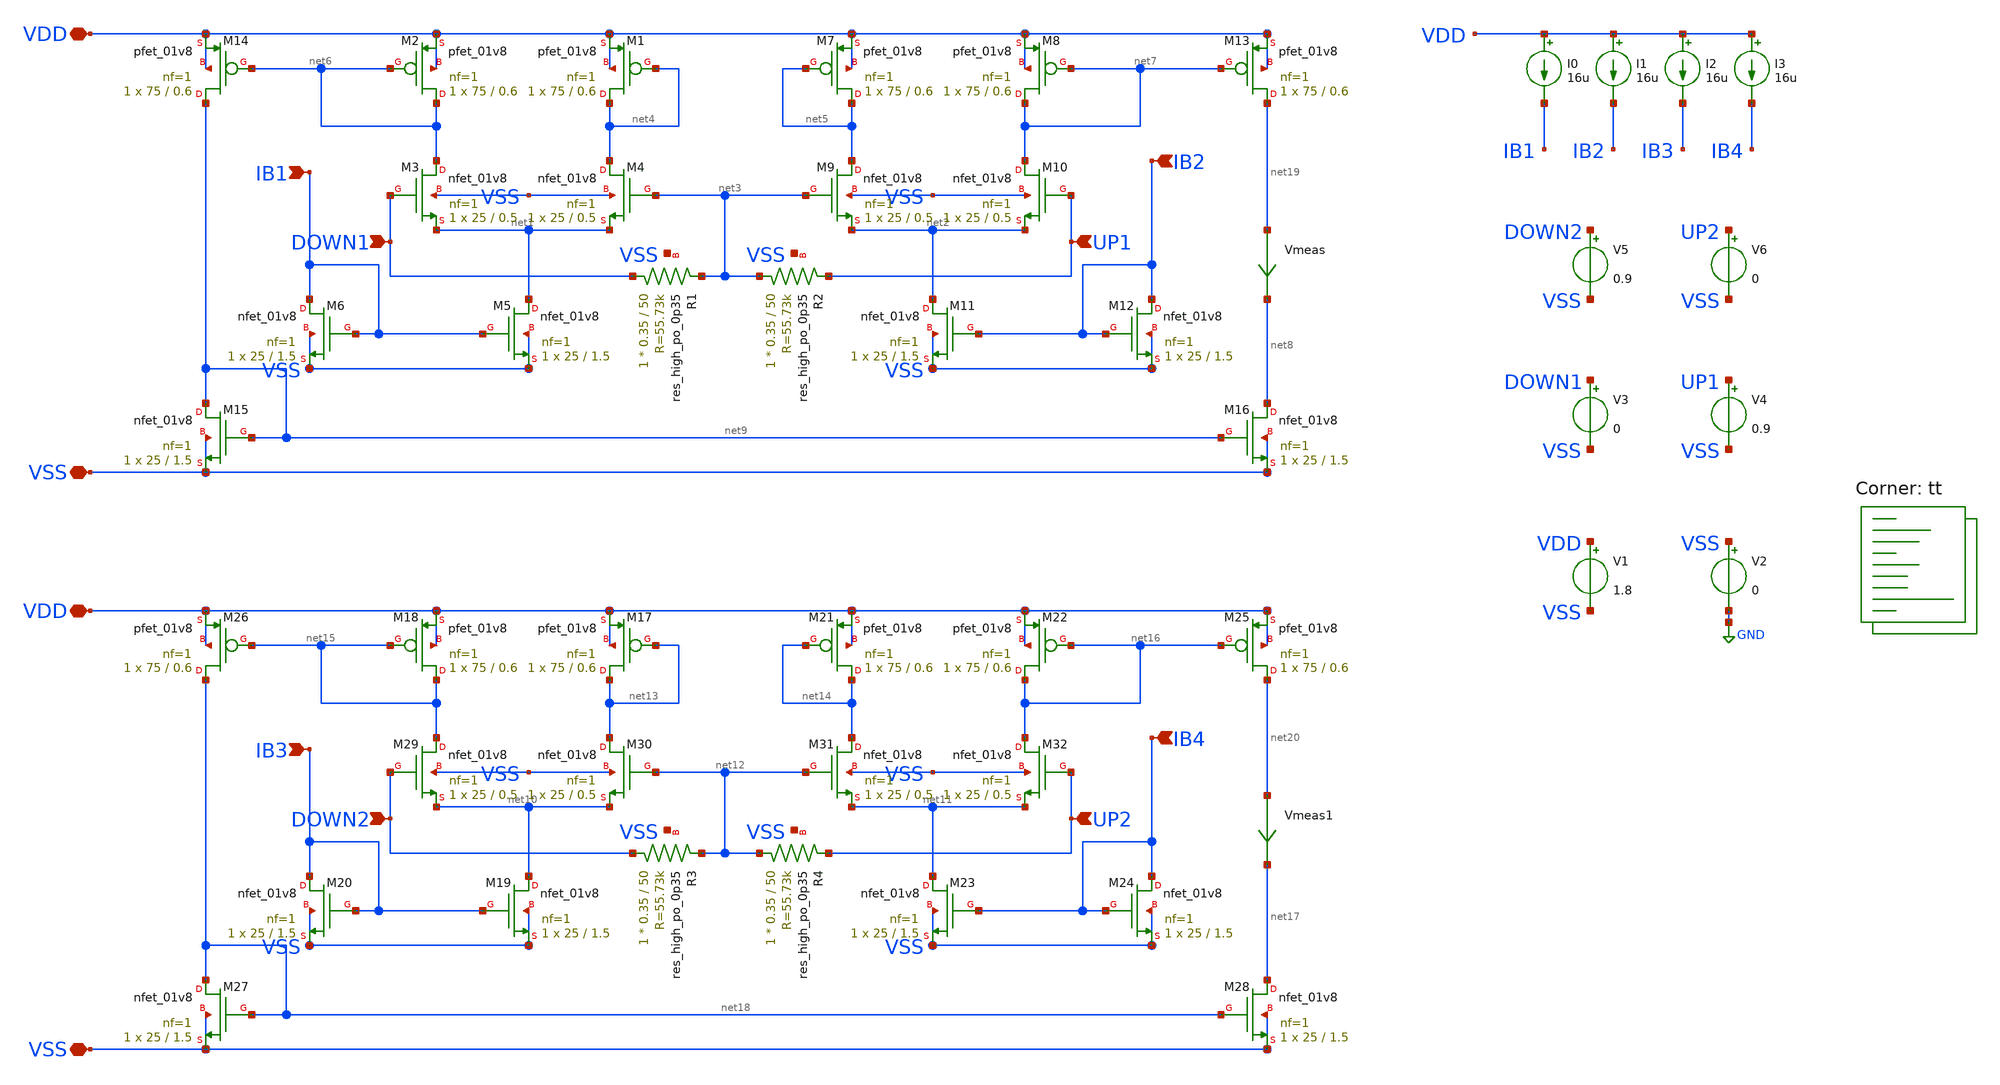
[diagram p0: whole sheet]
** sch_path: v-i-converter/current-transfer-function.sch
**.subckt current-transfer-function VDD VSS IB2 UP1 DOWN1 IB1 VDD VSS IB4 UP2 DOWN2 IB3
*.iopin VDD
*.iopin VSS
*.ipin IB2
*.ipin UP1
*.ipin DOWN1
*.ipin IB1
*.iopin VDD
*.iopin VSS
*.ipin IB4
*.ipin UP2
*.ipin DOWN2
*.ipin IB3
XM1 net4 net4 VDD VDD sky130_fd_pr__pfet_01v8 L=0.6 W=75 nf=1 ad='int((nf+1)/2) * W/nf * 0.29' as='int((nf+2)/2) * W/nf * 0.29'
+ pd='2*int((nf+1)/2) * (W/nf + 0.29)' ps='2*int((nf+2)/2) * (W/nf + 0.29)' nrd='0.29 / W' nrs='0.29 / W'
+ sa=0 sb=0 sd=0 mult=1 m=1
XM2 net6 net6 VDD VDD sky130_fd_pr__pfet_01v8 L=0.6 W=75 nf=1 ad='int((nf+1)/2) * W/nf * 0.29' as='int((nf+2)/2) * W/nf * 0.29'
+ pd='2*int((nf+1)/2) * (W/nf + 0.29)' ps='2*int((nf+2)/2) * (W/nf + 0.29)' nrd='0.29 / W' nrs='0.29 / W'
+ sa=0 sb=0 sd=0 mult=1 m=1
XM5 net1 IB1 VSS VSS sky130_fd_pr__nfet_01v8 L=1.5 W=25 nf=1 ad='int((nf+1)/2) * W/nf * 0.29' as='int((nf+2)/2) * W/nf * 0.29'
+ pd='2*int((nf+1)/2) * (W/nf + 0.29)' ps='2*int((nf+2)/2) * (W/nf + 0.29)' nrd='0.29 / W' nrs='0.29 / W'
+ sa=0 sb=0 sd=0 mult=1 m=1
XM6 IB1 IB1 VSS VSS sky130_fd_pr__nfet_01v8 L=1.5 W=25 nf=1 ad='int((nf+1)/2) * W/nf * 0.29' as='int((nf+2)/2) * W/nf * 0.29'
+ pd='2*int((nf+1)/2) * (W/nf + 0.29)' ps='2*int((nf+2)/2) * (W/nf + 0.29)' nrd='0.29 / W' nrs='0.29 / W'
+ sa=0 sb=0 sd=0 mult=1 m=1
XM7 net5 net5 VDD VDD sky130_fd_pr__pfet_01v8 L=0.6 W=75 nf=1 ad='int((nf+1)/2) * W/nf * 0.29' as='int((nf+2)/2) * W/nf * 0.29'
+ pd='2*int((nf+1)/2) * (W/nf + 0.29)' ps='2*int((nf+2)/2) * (W/nf + 0.29)' nrd='0.29 / W' nrs='0.29 / W'
+ sa=0 sb=0 sd=0 mult=1 m=1
XM8 net7 net7 VDD VDD sky130_fd_pr__pfet_01v8 L=0.6 W=75 nf=1 ad='int((nf+1)/2) * W/nf * 0.29' as='int((nf+2)/2) * W/nf * 0.29'
+ pd='2*int((nf+1)/2) * (W/nf + 0.29)' ps='2*int((nf+2)/2) * (W/nf + 0.29)' nrd='0.29 / W' nrs='0.29 / W'
+ sa=0 sb=0 sd=0 mult=1 m=1
XM11 net2 IB2 VSS VSS sky130_fd_pr__nfet_01v8 L=1.5 W=25 nf=1 ad='int((nf+1)/2) * W/nf * 0.29' as='int((nf+2)/2) * W/nf * 0.29'
+ pd='2*int((nf+1)/2) * (W/nf + 0.29)' ps='2*int((nf+2)/2) * (W/nf + 0.29)' nrd='0.29 / W' nrs='0.29 / W'
+ sa=0 sb=0 sd=0 mult=1 m=1
XM12 IB2 IB2 VSS VSS sky130_fd_pr__nfet_01v8 L=1.5 W=25 nf=1 ad='int((nf+1)/2) * W/nf * 0.29' as='int((nf+2)/2) * W/nf * 0.29'
+ pd='2*int((nf+1)/2) * (W/nf + 0.29)' ps='2*int((nf+2)/2) * (W/nf + 0.29)' nrd='0.29 / W' nrs='0.29 / W'
+ sa=0 sb=0 sd=0 mult=1 m=1
XM13 net19 net7 VDD VDD sky130_fd_pr__pfet_01v8 L=0.6 W=75 nf=1 ad='int((nf+1)/2) * W/nf * 0.29' as='int((nf+2)/2) * W/nf * 0.29'
+ pd='2*int((nf+1)/2) * (W/nf + 0.29)' ps='2*int((nf+2)/2) * (W/nf + 0.29)' nrd='0.29 / W' nrs='0.29 / W'
+ sa=0 sb=0 sd=0 mult=1 m=1
XM14 net9 net6 VDD VDD sky130_fd_pr__pfet_01v8 L=0.6 W=75 nf=1 ad='int((nf+1)/2) * W/nf * 0.29' as='int((nf+2)/2) * W/nf * 0.29'
+ pd='2*int((nf+1)/2) * (W/nf + 0.29)' ps='2*int((nf+2)/2) * (W/nf + 0.29)' nrd='0.29 / W' nrs='0.29 / W'
+ sa=0 sb=0 sd=0 mult=1 m=1
XM15 net9 net9 VSS VSS sky130_fd_pr__nfet_01v8 L=1.5 W=25 nf=1 ad='int((nf+1)/2) * W/nf * 0.29' as='int((nf+2)/2) * W/nf * 0.29'
+ pd='2*int((nf+1)/2) * (W/nf + 0.29)' ps='2*int((nf+2)/2) * (W/nf + 0.29)' nrd='0.29 / W' nrs='0.29 / W'
+ sa=0 sb=0 sd=0 mult=1 m=1
XM16 net8 net9 VSS VSS sky130_fd_pr__nfet_01v8 L=1.5 W=25 nf=1 ad='int((nf+1)/2) * W/nf * 0.29' as='int((nf+2)/2) * W/nf * 0.29'
+ pd='2*int((nf+1)/2) * (W/nf + 0.29)' ps='2*int((nf+2)/2) * (W/nf + 0.29)' nrd='0.29 / W' nrs='0.29 / W'
+ sa=0 sb=0 sd=0 mult=1 m=1
XR1 DOWN1 net3 VSS sky130_fd_pr__res_high_po_0p35 L=50 mult=1 m=1
XR2 net3 UP1 VSS sky130_fd_pr__res_high_po_0p35 L=50 mult=1 m=1
XM3 net6 DOWN1 net1 VSS sky130_fd_pr__nfet_01v8 L=0.5 W=25 nf=1 ad='int((nf+1)/2) * W/nf * 0.29' as='int((nf+2)/2) * W/nf * 0.29'
+ pd='2*int((nf+1)/2) * (W/nf + 0.29)' ps='2*int((nf+2)/2) * (W/nf + 0.29)' nrd='0.29 / W' nrs='0.29 / W'
+ sa=0 sb=0 sd=0 mult=1 m=1
XM4 net4 net3 net1 VSS sky130_fd_pr__nfet_01v8 L=0.5 W=25 nf=1 ad='int((nf+1)/2) * W/nf * 0.29' as='int((nf+2)/2) * W/nf * 0.29'
+ pd='2*int((nf+1)/2) * (W/nf + 0.29)' ps='2*int((nf+2)/2) * (W/nf + 0.29)' nrd='0.29 / W' nrs='0.29 / W'
+ sa=0 sb=0 sd=0 mult=1 m=1
XM9 net5 net3 net2 VSS sky130_fd_pr__nfet_01v8 L=0.5 W=25 nf=1 ad='int((nf+1)/2) * W/nf * 0.29' as='int((nf+2)/2) * W/nf * 0.29'
+ pd='2*int((nf+1)/2) * (W/nf + 0.29)' ps='2*int((nf+2)/2) * (W/nf + 0.29)' nrd='0.29 / W' nrs='0.29 / W'
+ sa=0 sb=0 sd=0 mult=1 m=1
XM10 net7 UP1 net2 VSS sky130_fd_pr__nfet_01v8 L=0.5 W=25 nf=1 ad='int((nf+1)/2) * W/nf * 0.29' as='int((nf+2)/2) * W/nf * 0.29'
+ pd='2*int((nf+1)/2) * (W/nf + 0.29)' ps='2*int((nf+2)/2) * (W/nf + 0.29)' nrd='0.29 / W' nrs='0.29 / W'
+ sa=0 sb=0 sd=0 mult=1 m=1
XM17 net13 net13 VDD VDD sky130_fd_pr__pfet_01v8 L=0.6 W=75 nf=1 ad='int((nf+1)/2) * W/nf * 0.29' as='int((nf+2)/2) * W/nf * 0.29'
+ pd='2*int((nf+1)/2) * (W/nf + 0.29)' ps='2*int((nf+2)/2) * (W/nf + 0.29)' nrd='0.29 / W' nrs='0.29 / W'
+ sa=0 sb=0 sd=0 mult=1 m=1
XM18 net15 net15 VDD VDD sky130_fd_pr__pfet_01v8 L=0.6 W=75 nf=1 ad='int((nf+1)/2) * W/nf * 0.29' as='int((nf+2)/2) * W/nf * 0.29'
+ pd='2*int((nf+1)/2) * (W/nf + 0.29)' ps='2*int((nf+2)/2) * (W/nf + 0.29)' nrd='0.29 / W' nrs='0.29 / W'
+ sa=0 sb=0 sd=0 mult=1 m=1
XM19 net10 IB3 VSS VSS sky130_fd_pr__nfet_01v8 L=1.5 W=25 nf=1 ad='int((nf+1)/2) * W/nf * 0.29' as='int((nf+2)/2) * W/nf * 0.29'
+ pd='2*int((nf+1)/2) * (W/nf + 0.29)' ps='2*int((nf+2)/2) * (W/nf + 0.29)' nrd='0.29 / W' nrs='0.29 / W'
+ sa=0 sb=0 sd=0 mult=1 m=1
XM20 IB3 IB3 VSS VSS sky130_fd_pr__nfet_01v8 L=1.5 W=25 nf=1 ad='int((nf+1)/2) * W/nf * 0.29' as='int((nf+2)/2) * W/nf * 0.29'
+ pd='2*int((nf+1)/2) * (W/nf + 0.29)' ps='2*int((nf+2)/2) * (W/nf + 0.29)' nrd='0.29 / W' nrs='0.29 / W'
+ sa=0 sb=0 sd=0 mult=1 m=1
XM21 net14 net14 VDD VDD sky130_fd_pr__pfet_01v8 L=0.6 W=75 nf=1 ad='int((nf+1)/2) * W/nf * 0.29' as='int((nf+2)/2) * W/nf * 0.29'
+ pd='2*int((nf+1)/2) * (W/nf + 0.29)' ps='2*int((nf+2)/2) * (W/nf + 0.29)' nrd='0.29 / W' nrs='0.29 / W'
+ sa=0 sb=0 sd=0 mult=1 m=1
XM22 net16 net16 VDD VDD sky130_fd_pr__pfet_01v8 L=0.6 W=75 nf=1 ad='int((nf+1)/2) * W/nf * 0.29' as='int((nf+2)/2) * W/nf * 0.29'
+ pd='2*int((nf+1)/2) * (W/nf + 0.29)' ps='2*int((nf+2)/2) * (W/nf + 0.29)' nrd='0.29 / W' nrs='0.29 / W'
+ sa=0 sb=0 sd=0 mult=1 m=1
XM23 net11 IB4 VSS VSS sky130_fd_pr__nfet_01v8 L=1.5 W=25 nf=1 ad='int((nf+1)/2) * W/nf * 0.29' as='int((nf+2)/2) * W/nf * 0.29'
+ pd='2*int((nf+1)/2) * (W/nf + 0.29)' ps='2*int((nf+2)/2) * (W/nf + 0.29)' nrd='0.29 / W' nrs='0.29 / W'
+ sa=0 sb=0 sd=0 mult=1 m=1
XM24 IB4 IB4 VSS VSS sky130_fd_pr__nfet_01v8 L=1.5 W=25 nf=1 ad='int((nf+1)/2) * W/nf * 0.29' as='int((nf+2)/2) * W/nf * 0.29'
+ pd='2*int((nf+1)/2) * (W/nf + 0.29)' ps='2*int((nf+2)/2) * (W/nf + 0.29)' nrd='0.29 / W' nrs='0.29 / W'
+ sa=0 sb=0 sd=0 mult=1 m=1
XM25 net20 net16 VDD VDD sky130_fd_pr__pfet_01v8 L=0.6 W=75 nf=1 ad='int((nf+1)/2) * W/nf * 0.29' as='int((nf+2)/2) * W/nf * 0.29'
+ pd='2*int((nf+1)/2) * (W/nf + 0.29)' ps='2*int((nf+2)/2) * (W/nf + 0.29)' nrd='0.29 / W' nrs='0.29 / W'
+ sa=0 sb=0 sd=0 mult=1 m=1
XM26 net18 net15 VDD VDD sky130_fd_pr__pfet_01v8 L=0.6 W=75 nf=1 ad='int((nf+1)/2) * W/nf * 0.29' as='int((nf+2)/2) * W/nf * 0.29'
+ pd='2*int((nf+1)/2) * (W/nf + 0.29)' ps='2*int((nf+2)/2) * (W/nf + 0.29)' nrd='0.29 / W' nrs='0.29 / W'
+ sa=0 sb=0 sd=0 mult=1 m=1
XM27 net18 net18 VSS VSS sky130_fd_pr__nfet_01v8 L=1.5 W=25 nf=1 ad='int((nf+1)/2) * W/nf * 0.29' as='int((nf+2)/2) * W/nf * 0.29'
+ pd='2*int((nf+1)/2) * (W/nf + 0.29)' ps='2*int((nf+2)/2) * (W/nf + 0.29)' nrd='0.29 / W' nrs='0.29 / W'
+ sa=0 sb=0 sd=0 mult=1 m=1
XM28 net17 net18 VSS VSS sky130_fd_pr__nfet_01v8 L=1.5 W=25 nf=1 ad='int((nf+1)/2) * W/nf * 0.29' as='int((nf+2)/2) * W/nf * 0.29'
+ pd='2*int((nf+1)/2) * (W/nf + 0.29)' ps='2*int((nf+2)/2) * (W/nf + 0.29)' nrd='0.29 / W' nrs='0.29 / W'
+ sa=0 sb=0 sd=0 mult=1 m=1
XR3 DOWN2 net12 VSS sky130_fd_pr__res_high_po_0p35 L=50 mult=1 m=1
XR4 net12 UP2 VSS sky130_fd_pr__res_high_po_0p35 L=50 mult=1 m=1
XM29 net15 DOWN2 net10 VSS sky130_fd_pr__nfet_01v8 L=0.5 W=25 nf=1 ad='int((nf+1)/2) * W/nf * 0.29' as='int((nf+2)/2) * W/nf * 0.29'
+ pd='2*int((nf+1)/2) * (W/nf + 0.29)' ps='2*int((nf+2)/2) * (W/nf + 0.29)' nrd='0.29 / W' nrs='0.29 / W'
+ sa=0 sb=0 sd=0 mult=1 m=1
XM30 net13 net12 net10 VSS sky130_fd_pr__nfet_01v8 L=0.5 W=25 nf=1 ad='int((nf+1)/2) * W/nf * 0.29' as='int((nf+2)/2) * W/nf * 0.29'
+ pd='2*int((nf+1)/2) * (W/nf + 0.29)' ps='2*int((nf+2)/2) * (W/nf + 0.29)' nrd='0.29 / W' nrs='0.29 / W'
+ sa=0 sb=0 sd=0 mult=1 m=1
XM31 net14 net12 net11 VSS sky130_fd_pr__nfet_01v8 L=0.5 W=25 nf=1 ad='int((nf+1)/2) * W/nf * 0.29' as='int((nf+2)/2) * W/nf * 0.29'
+ pd='2*int((nf+1)/2) * (W/nf + 0.29)' ps='2*int((nf+2)/2) * (W/nf + 0.29)' nrd='0.29 / W' nrs='0.29 / W'
+ sa=0 sb=0 sd=0 mult=1 m=1
XM32 net16 UP2 net11 VSS sky130_fd_pr__nfet_01v8 L=0.5 W=25 nf=1 ad='int((nf+1)/2) * W/nf * 0.29' as='int((nf+2)/2) * W/nf * 0.29'
+ pd='2*int((nf+1)/2) * (W/nf + 0.29)' ps='2*int((nf+2)/2) * (W/nf + 0.29)' nrd='0.29 / W' nrs='0.29 / W'
+ sa=0 sb=0 sd=0 mult=1 m=1
Vmeas net19 net8 0
.save i(vmeas)
Vmeas1 net20 net17 0
.save i(vmeas1)
V1 VDD VSS 1.8
V2 VSS GND 0
V3 DOWN1 VSS 0
V4 UP1 VSS 0.9
V5 DOWN2 VSS 0.9
V6 UP2 VSS 0
I0 VDD IB1 16u
I1 VDD IB2 16u
I2 VDD IB3 16u
I3 VDD IB4 16u
**** begin user architecture code
.lib $::SKYWATER_MODELS/sky130.lib.spice tt



.control

* --- Sweep DOWN (up input fixed at 0.9V) ---
dc V3 0 1.8 0.001
plot i(Vmeas)

* --- Sweep UP (down input fixed at 0.9V) ---
dc V6 0 1.8 0.001
plot i(Vmeas1)

.endc


**** end user architecture code
**.ends
.GLOBAL GND
.end
